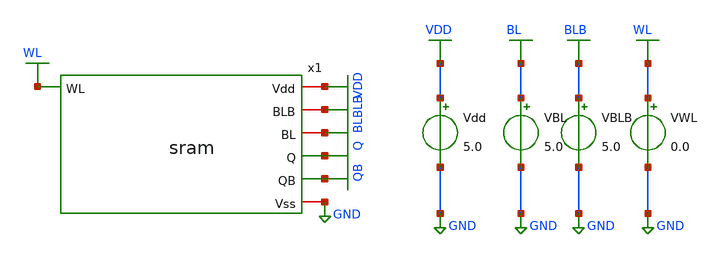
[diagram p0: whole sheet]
** sch_path: sram_tb_dc_read_wl.sch
**.subckt sram_tb_dc_read_wl
Vdd VDD GND 5.0
VBL BL GND 5.0
VBLB BLB GND 5.0
VWL WL GND 0.0
x1 WL VDD BLB BL Q QB GND sram
**** begin user architecture code
 .include $::LIB/ip62_models


* DC read-disturb test.
* Both bitlines are held at 5 V (worst-case sustained precharge).
* Follow the stored state Q=0 V, QB=5 V while sweeping WL.
.nodeset v(Q)=0 v(QB)=5

.control
save v(WL) v(Q) v(QB)

dc VWL 0 5 0.01

meas dc Q_DISTURB_MAX max v(Q)
meas dc QB_DROOP_MIN min v(QB)

plot v(Q) v(QB) xlabel 'WL voltage (V)' ylabel 'Storage-node voltage (V)' ylimit -0.2 5.2 title 'DC READ DISTURB: Q=0, QB=5'
.endc


**** end user architecture code
**.ends

* expanding   symbol:  sram.sym # of pins=7
** sym_path: sram.sym
** sch_path: sram.sch
.subckt sram WL Vdd BLB BL Q QB Vss
*.iopin Vdd
*.iopin Vss
*.iopin BLB
*.iopin BL
*.ipin WL
*.opin Q
*.opin QB
XXM1 Q QB Vss Vss NMOS w=3.4u l=1u nrd=0 nrs=0 m=1
XXM2 Q QB Vdd Vdd PMOS w=3.4u l=1u nrd=0 nrs=0 m=1
XXM3 QB Q Vss Vss NMOS w=3.4u l=1u nrd=0 nrs=0 m=1
XXM4 QB Q Vdd Vdd PMOS w=3.4u l=1u nrd=0 nrs=0 m=1
XXM7 Q WL BL Vss NMOS w=3.4u l=1u nrd=0 nrs=0 m=1
XXM6 QB WL BLB Vss NMOS w=3.4u l=1u nrd=0 nrs=0 m=1
.ends

.GLOBAL VDD
.GLOBAL GND
.GLOBAL QB
.GLOBAL Q
.GLOBAL BLB
.GLOBAL BL
.GLOBAL WL
.end
